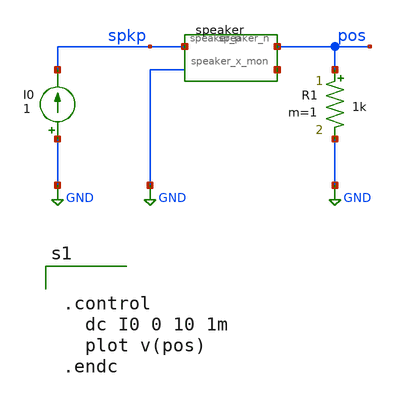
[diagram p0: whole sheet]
** sch_path: examples/analog_speaker/dc.sch
**.subckt dc
R1 pos GND 1k m=1
I0 GND spkp 1
Xspeaker1 spkp pos net1 speaker
**** begin user architecture code


.control
  dc I0 0 10 1m
  plot v(pos)
.endc


**** end user architecture code
**.ends

* expanding   symbol:  speaker.sym # of pins=3
** sym_path: examples/analog_speaker/speaker.sym
.include /workspace/speaker.spice
.GLOBAL GND
.end
